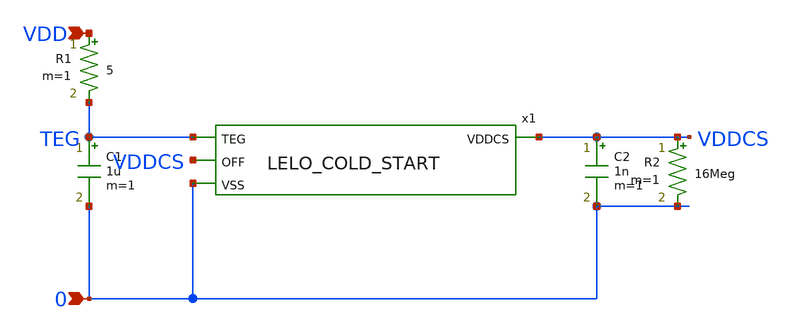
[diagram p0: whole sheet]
** sch_path: design/LELO_SVOD_SKY130A/LELO_COLD_START_TB.sch
**.subckt LELO_COLD_START_TB VDD 0
*.ipin VDD
*.ipin 0
x1 TEG VDDCS VDDCS 0 LELO_COLD_START
R1 VDD TEG 5 m=1
C1 TEG 0 1u m=1
C2 VDDCS 0 1n m=1
R2 VDDCS 0 16Meg m=1
**.ends

* expanding   symbol:  LELO_SVOD_SKY130A/LELO_COLD_START.sym # of pins=4
** sym_path: design/LELO_SVOD_SKY130A/LELO_COLD_START.sym
** sch_path: design/LELO_SVOD_SKY130A/LELO_COLD_START.sch
.subckt LELO_COLD_START TEG VDDCS OFF VSS
*.ipin VSS
*.ipin TEG
*.opin VDDCS
*.ipin OFF
C2 net4 VG1 10p m=1
x1 VG2 net2 1812PS-564_imp
x2 net1 VG1 1812PS-564_imp
C4 net5 VG2 10p m=1
XM1 net1 VG2 net3 net3 sky130_fd_pr__nfet_20v0_zvt W=60 L=0.5 m=100
XM2 net2 VG1 net3 net3 sky130_fd_pr__nfet_20v0_zvt W=60 L=0.5 m=100
XM3 TEG TEG net4 TEG sky130_fd_pr__nfet_01v8_lvt L=0.15 W=100 nf=1 ad='int((1 + 1)/2) * 100 / 1 * 0.29'
+ as='int((1 + 2)/2) * 100 / 1 * 0.29' pd='2*int((1 + 1)/2) * (100 / 1 + 0.29)' ps='2*int((1 + 2)/2) * (100 / 1 + 0.29)'
+ nrd='0.29 / 100 ' nrs='0.29 / 100 ' sa=0 sb=0 sd=0 mult=1 m=1
XM7 net4 net4 net5 net4 sky130_fd_pr__nfet_01v8_lvt L=0.15 W=100 nf=1 ad='int((1 + 1)/2) * 100 / 1 * 0.29'
+ as='int((1 + 2)/2) * 100 / 1 * 0.29' pd='2*int((1 + 1)/2) * (100 / 1 + 0.29)' ps='2*int((1 + 2)/2) * (100 / 1 + 0.29)'
+ nrd='0.29 / 100 ' nrs='0.29 / 100 ' sa=0 sb=0 sd=0 mult=1 m=1
XM8 net5 net5 VDDCS net5 sky130_fd_pr__nfet_01v8_lvt L=0.15 W=100 nf=1 ad='int((1 + 1)/2) * 100 / 1 * 0.29'
+ as='int((1 + 2)/2) * 100 / 1 * 0.29' pd='2*int((1 + 1)/2) * (100 / 1 + 0.29)' ps='2*int((1 + 2)/2) * (100 / 1 + 0.29)'
+ nrd='0.29 / 100 ' nrs='0.29 / 100 ' sa=0 sb=0 sd=0 mult=1 m=1
XM4 net3 OFF VSS VSS sky130_fd_pr__nfet_20v0_zvt W=60 L=0.5 m=200
x3 TEG net1 1812PS-332_imp
x4 TEG net2 1812PS-332_imp
.ends


* expanding   symbol:  LELO_SVOD_SKY130A/1812PS-564_imp.sym # of pins=2
** sym_path: design/LELO_SVOD_SKY130A/1812PS-564_imp.sym

.subckt 1812PS-564_imp port1 port2
X1 port1 port2 Model1D R1=70 R2=6.1 C= 7.71p K1=0.000001 K2=115.8 K3= 560u K4=0.000001 K5=0.000001
+ L=0 Is=0 a=0 L_Z0=0 L_EL=0 L_F0=0E6 PkZ=153558.837
.ends 1812PS-564_imp

* expanding   symbol:  LELO_SVOD_SKY130A/1812PS-332_imp.sym # of pins=2
** sym_path: design/LELO_SVOD_SKY130A/1812PS-332_imp.sym

.subckt 1812PS-332_imp port1 port2
X1 port1 port2 Model1D R1=35 R2=0.09 C= 0.27p K1=0.000001 K2=0.22 K3= 3.3u K4=0.000001 K5=0.0000515
+ L=0 Is=0 a=0 L_Z0=0 L_EL=0 L_F0=0E6 PkZ=2833.59737
.ends 1812PS-332_imp
.end
